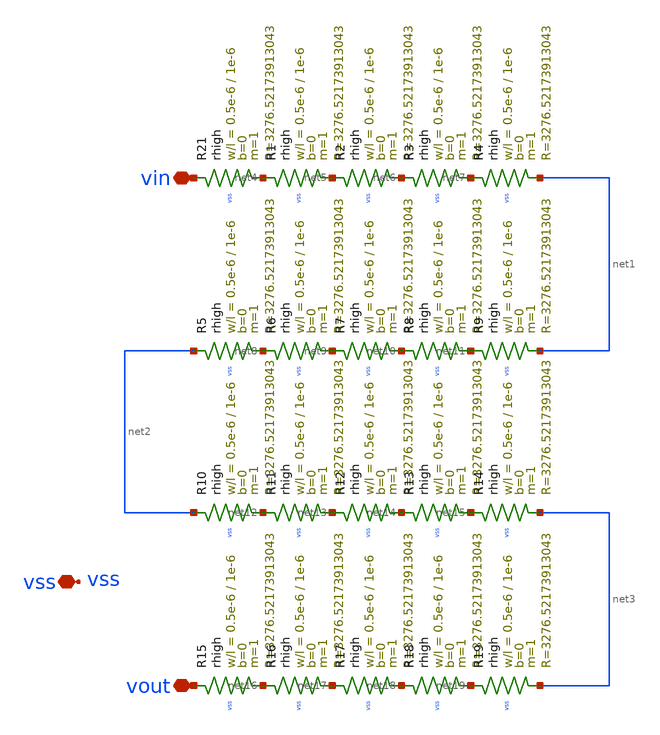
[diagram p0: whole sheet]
** sch_path: LVS/Unic_cass_final_design_lvs/Simulations/Opamp_design/Src/res.sch
**.subckt res vin vout vss
*.iopin vin
*.iopin vout
*.iopin vss
XR21 vin net4 vss rhigh w=0.5e-6 l=1e-6 m=1 b=0 mm_ok=1
XR1 net4 net5 vss rhigh w=0.5e-6 l=1e-6 m=1 b=0 mm_ok=1
XR2 net5 net6 vss rhigh w=0.5e-6 l=1e-6 m=1 b=0 mm_ok=1
XR3 net6 net7 vss rhigh w=0.5e-6 l=1e-6 m=1 b=0 mm_ok=1
XR4 net7 net1 vss rhigh w=0.5e-6 l=1e-6 m=1 b=0 mm_ok=1
XR5 net2 net8 vss rhigh w=0.5e-6 l=1e-6 m=1 b=0 mm_ok=1
XR6 net8 net9 vss rhigh w=0.5e-6 l=1e-6 m=1 b=0 mm_ok=1
XR7 net9 net10 vss rhigh w=0.5e-6 l=1e-6 m=1 b=0 mm_ok=1
XR8 net10 net11 vss rhigh w=0.5e-6 l=1e-6 m=1 b=0 mm_ok=1
XR9 net11 net1 vss rhigh w=0.5e-6 l=1e-6 m=1 b=0 mm_ok=1
XR10 net2 net12 vss rhigh w=0.5e-6 l=1e-6 m=1 b=0 mm_ok=1
XR11 net12 net13 vss rhigh w=0.5e-6 l=1e-6 m=1 b=0 mm_ok=1
XR12 net13 net14 vss rhigh w=0.5e-6 l=1e-6 m=1 b=0 mm_ok=1
XR13 net14 net15 vss rhigh w=0.5e-6 l=1e-6 m=1 b=0 mm_ok=1
XR14 net15 net3 vss rhigh w=0.5e-6 l=1e-6 m=1 b=0 mm_ok=1
XR15 vout net16 vss rhigh w=0.5e-6 l=1e-6 m=1 b=0 mm_ok=1
XR16 net16 net17 vss rhigh w=0.5e-6 l=1e-6 m=1 b=0 mm_ok=1
XR17 net17 net18 vss rhigh w=0.5e-6 l=1e-6 m=1 b=0 mm_ok=1
XR18 net18 net19 vss rhigh w=0.5e-6 l=1e-6 m=1 b=0 mm_ok=1
XR19 net19 net3 vss rhigh w=0.5e-6 l=1e-6 m=1 b=0 mm_ok=1
**.ends
.end
